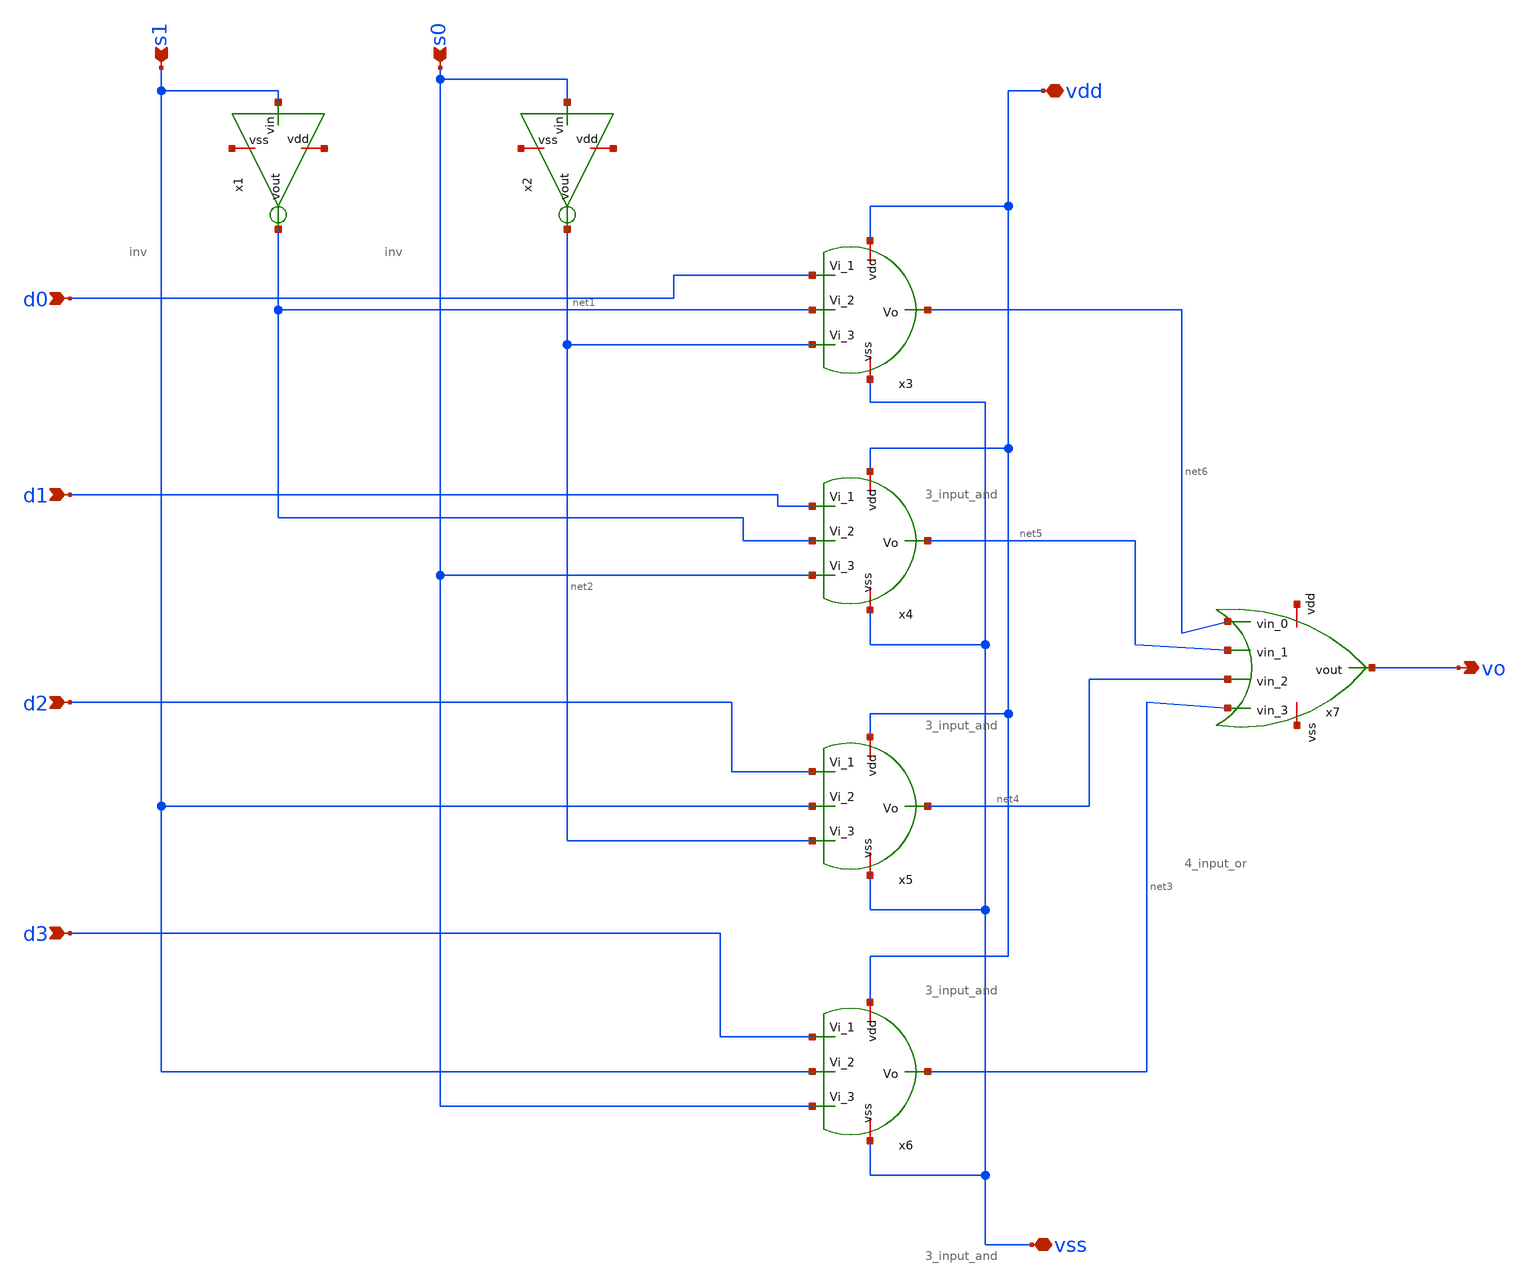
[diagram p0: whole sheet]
** sch_path: designs/4x1_mux.sch
**.subckt 4x1_mux d0 d1 d2 d3 s1 s0 vdd vss vo
*.ipin d0
*.ipin d1
*.ipin d2
*.ipin d3
*.ipin s1
*.ipin s0
*.iopin vdd
*.iopin vss
*.opin vo
x1 net7 s1 net1 net8 inv
x2 net9 s0 net2 net10 inv
x3 vdd net6 d0 net1 net2 vss 3_input_and
x4 vdd net5 d1 net1 s0 vss 3_input_and
x5 vdd net4 d2 s1 net2 vss 3_input_and
x6 vdd net3 d3 s1 s0 vss 3_input_and
x7 net11 net6 net5 net4 net3 vo net12 4_input_or
**.ends

* expanding   symbol:  inv.sym # of pins=4
** sym_path: designs/inv.sym
** sch_path: designs/inv.sch
.subckt inv vdd vin vout vss
*.iopin vdd
*.iopin vss
*.ipin vin
*.opin vout
XM1 vout vin vdd vdd pfet_03v3 L=0.28u W=0.22u nf=1 ad='int((nf+1)/2) * W/nf * 0.18u' as='int((nf+2)/2) * W/nf * 0.18u'
+ pd='2*int((nf+1)/2) * (W/nf + 0.18u)' ps='2*int((nf+2)/2) * (W/nf + 0.18u)' nrd='0.18u / W' nrs='0.18u / W'
+ sa=0 sb=0 sd=0 m=1
XM2 vout vin vss vss nfet_03v3 L=0.28u W=0.22u nf=1 ad='int((nf+1)/2) * W/nf * 0.18u' as='int((nf+2)/2) * W/nf * 0.18u'
+ pd='2*int((nf+1)/2) * (W/nf + 0.18u)' ps='2*int((nf+2)/2) * (W/nf + 0.18u)' nrd='0.18u / W' nrs='0.18u / W'
+ sa=0 sb=0 sd=0 m=1
.ends


* expanding   symbol:  3_input_and.sym # of pins=6
** sym_path: designs/3_input_and.sym
** sch_path: designs/3_input_and.sch
.subckt 3_input_and vdd Vo Vi_1 Vi_2 Vi_3 vss
*.iopin vdd
*.iopin vss
*.ipin Vi_1
*.ipin Vi_2
*.ipin Vi_3
*.opin Vo
XM1 net1 Vi_1 vdd vdd pfet_03v3 L=0.28u W=0.22u nf=1 ad='int((nf+1)/2) * W/nf * 0.18u' as='int((nf+2)/2) * W/nf * 0.18u'
+ pd='2*int((nf+1)/2) * (W/nf + 0.18u)' ps='2*int((nf+2)/2) * (W/nf + 0.18u)' nrd='0.18u / W' nrs='0.18u / W'
+ sa=0 sb=0 sd=0 m=1
XM2 net1 Vi_2 vdd vdd pfet_03v3 L=0.28u W=0.22u nf=1 ad='int((nf+1)/2) * W/nf * 0.18u' as='int((nf+2)/2) * W/nf * 0.18u'
+ pd='2*int((nf+1)/2) * (W/nf + 0.18u)' ps='2*int((nf+2)/2) * (W/nf + 0.18u)' nrd='0.18u / W' nrs='0.18u / W'
+ sa=0 sb=0 sd=0 m=1
XM3 net1 Vi_3 vdd vdd pfet_03v3 L=0.28u W=0.22u nf=1 ad='int((nf+1)/2) * W/nf * 0.18u' as='int((nf+2)/2) * W/nf * 0.18u'
+ pd='2*int((nf+1)/2) * (W/nf + 0.18u)' ps='2*int((nf+2)/2) * (W/nf + 0.18u)' nrd='0.18u / W' nrs='0.18u / W'
+ sa=0 sb=0 sd=0 m=1
XM4 net1 Vi_1 net3 vss nfet_03v3 L=0.28u W=0.22u nf=1 ad='int((nf+1)/2) * W/nf * 0.18u' as='int((nf+2)/2) * W/nf * 0.18u'
+ pd='2*int((nf+1)/2) * (W/nf + 0.18u)' ps='2*int((nf+2)/2) * (W/nf + 0.18u)' nrd='0.18u / W' nrs='0.18u / W'
+ sa=0 sb=0 sd=0 m=1
XM5 net3 Vi_2 net2 vss nfet_03v3 L=0.28u W=0.22u nf=1 ad='int((nf+1)/2) * W/nf * 0.18u' as='int((nf+2)/2) * W/nf * 0.18u'
+ pd='2*int((nf+1)/2) * (W/nf + 0.18u)' ps='2*int((nf+2)/2) * (W/nf + 0.18u)' nrd='0.18u / W' nrs='0.18u / W'
+ sa=0 sb=0 sd=0 m=1
XM6 net2 Vi_3 vss vss nfet_03v3 L=0.28u W=0.22u nf=1 ad='int((nf+1)/2) * W/nf * 0.18u' as='int((nf+2)/2) * W/nf * 0.18u'
+ pd='2*int((nf+1)/2) * (W/nf + 0.18u)' ps='2*int((nf+2)/2) * (W/nf + 0.18u)' nrd='0.18u / W' nrs='0.18u / W'
+ sa=0 sb=0 sd=0 m=1
XM7 Vo net1 vdd vdd pfet_03v3 L=0.28u W=0.22u nf=1 ad='int((nf+1)/2) * W/nf * 0.18u' as='int((nf+2)/2) * W/nf * 0.18u'
+ pd='2*int((nf+1)/2) * (W/nf + 0.18u)' ps='2*int((nf+2)/2) * (W/nf + 0.18u)' nrd='0.18u / W' nrs='0.18u / W'
+ sa=0 sb=0 sd=0 m=1
XM8 Vo net1 vss vss nfet_03v3 L=0.28u W=0.22u nf=1 ad='int((nf+1)/2) * W/nf * 0.18u' as='int((nf+2)/2) * W/nf * 0.18u'
+ pd='2*int((nf+1)/2) * (W/nf + 0.18u)' ps='2*int((nf+2)/2) * (W/nf + 0.18u)' nrd='0.18u / W' nrs='0.18u / W'
+ sa=0 sb=0 sd=0 m=1
.ends


* expanding   symbol:  4_input_or.sym # of pins=7
** sym_path: designs/4_input_or.sym
** sch_path: designs/4_input_or.sch
.subckt 4_input_or vdd vin_0 vin_1 vin_2 vin_3 vout vss
*.iopin vdd
*.iopin vss
*.ipin vin_0
*.ipin vin_1
*.ipin vin_2
*.ipin vin_3
*.opin vout
XM1 net1 vin_0 vdd vdd pfet_03v3 L=0.28u W=0.22u nf=1 ad='int((nf+1)/2) * W/nf * 0.18u' as='int((nf+2)/2) * W/nf * 0.18u'
+ pd='2*int((nf+1)/2) * (W/nf + 0.18u)' ps='2*int((nf+2)/2) * (W/nf + 0.18u)' nrd='0.18u / W' nrs='0.18u / W'
+ sa=0 sb=0 sd=0 m=1
XM2 net4 vin_3 vss vss nfet_03v3 L=0.28u W=0.22u nf=1 ad='int((nf+1)/2) * W/nf * 0.18u' as='int((nf+2)/2) * W/nf * 0.18u'
+ pd='2*int((nf+1)/2) * (W/nf + 0.18u)' ps='2*int((nf+2)/2) * (W/nf + 0.18u)' nrd='0.18u / W' nrs='0.18u / W'
+ sa=0 sb=0 sd=0 m=1
XM3 net2 vin_1 net1 vdd pfet_03v3 L=0.28u W=0.22u nf=1 ad='int((nf+1)/2) * W/nf * 0.18u' as='int((nf+2)/2) * W/nf * 0.18u'
+ pd='2*int((nf+1)/2) * (W/nf + 0.18u)' ps='2*int((nf+2)/2) * (W/nf + 0.18u)' nrd='0.18u / W' nrs='0.18u / W'
+ sa=0 sb=0 sd=0 m=1
XM4 net3 vin_2 net2 vdd pfet_03v3 L=0.28u W=0.22u nf=1 ad='int((nf+1)/2) * W/nf * 0.18u' as='int((nf+2)/2) * W/nf * 0.18u'
+ pd='2*int((nf+1)/2) * (W/nf + 0.18u)' ps='2*int((nf+2)/2) * (W/nf + 0.18u)' nrd='0.18u / W' nrs='0.18u / W'
+ sa=0 sb=0 sd=0 m=1
XM5 net4 vin_3 net3 vdd pfet_03v3 L=0.28u W=0.22u nf=1 ad='int((nf+1)/2) * W/nf * 0.18u' as='int((nf+2)/2) * W/nf * 0.18u'
+ pd='2*int((nf+1)/2) * (W/nf + 0.18u)' ps='2*int((nf+2)/2) * (W/nf + 0.18u)' nrd='0.18u / W' nrs='0.18u / W'
+ sa=0 sb=0 sd=0 m=1
XM6 net4 vin_2 vss vss nfet_03v3 L=0.28u W=0.22u nf=1 ad='int((nf+1)/2) * W/nf * 0.18u' as='int((nf+2)/2) * W/nf * 0.18u'
+ pd='2*int((nf+1)/2) * (W/nf + 0.18u)' ps='2*int((nf+2)/2) * (W/nf + 0.18u)' nrd='0.18u / W' nrs='0.18u / W'
+ sa=0 sb=0 sd=0 m=1
XM7 net4 vin_1 vss vss nfet_03v3 L=0.28u W=0.22u nf=1 ad='int((nf+1)/2) * W/nf * 0.18u' as='int((nf+2)/2) * W/nf * 0.18u'
+ pd='2*int((nf+1)/2) * (W/nf + 0.18u)' ps='2*int((nf+2)/2) * (W/nf + 0.18u)' nrd='0.18u / W' nrs='0.18u / W'
+ sa=0 sb=0 sd=0 m=1
XM8 net4 vin_0 vss vss nfet_03v3 L=0.28u W=0.22u nf=1 ad='int((nf+1)/2) * W/nf * 0.18u' as='int((nf+2)/2) * W/nf * 0.18u'
+ pd='2*int((nf+1)/2) * (W/nf + 0.18u)' ps='2*int((nf+2)/2) * (W/nf + 0.18u)' nrd='0.18u / W' nrs='0.18u / W'
+ sa=0 sb=0 sd=0 m=1
XM9 vout net4 vdd vdd pfet_03v3 L=0.28u W=0.22u nf=1 ad='int((nf+1)/2) * W/nf * 0.18u' as='int((nf+2)/2) * W/nf * 0.18u'
+ pd='2*int((nf+1)/2) * (W/nf + 0.18u)' ps='2*int((nf+2)/2) * (W/nf + 0.18u)' nrd='0.18u / W' nrs='0.18u / W'
+ sa=0 sb=0 sd=0 m=1
XM10 vout net4 vss vss nfet_03v3 L=0.28u W=0.22u nf=1 ad='int((nf+1)/2) * W/nf * 0.18u' as='int((nf+2)/2) * W/nf * 0.18u'
+ pd='2*int((nf+1)/2) * (W/nf + 0.18u)' ps='2*int((nf+2)/2) * (W/nf + 0.18u)' nrd='0.18u / W' nrs='0.18u / W'
+ sa=0 sb=0 sd=0 m=1
.ends

.end
